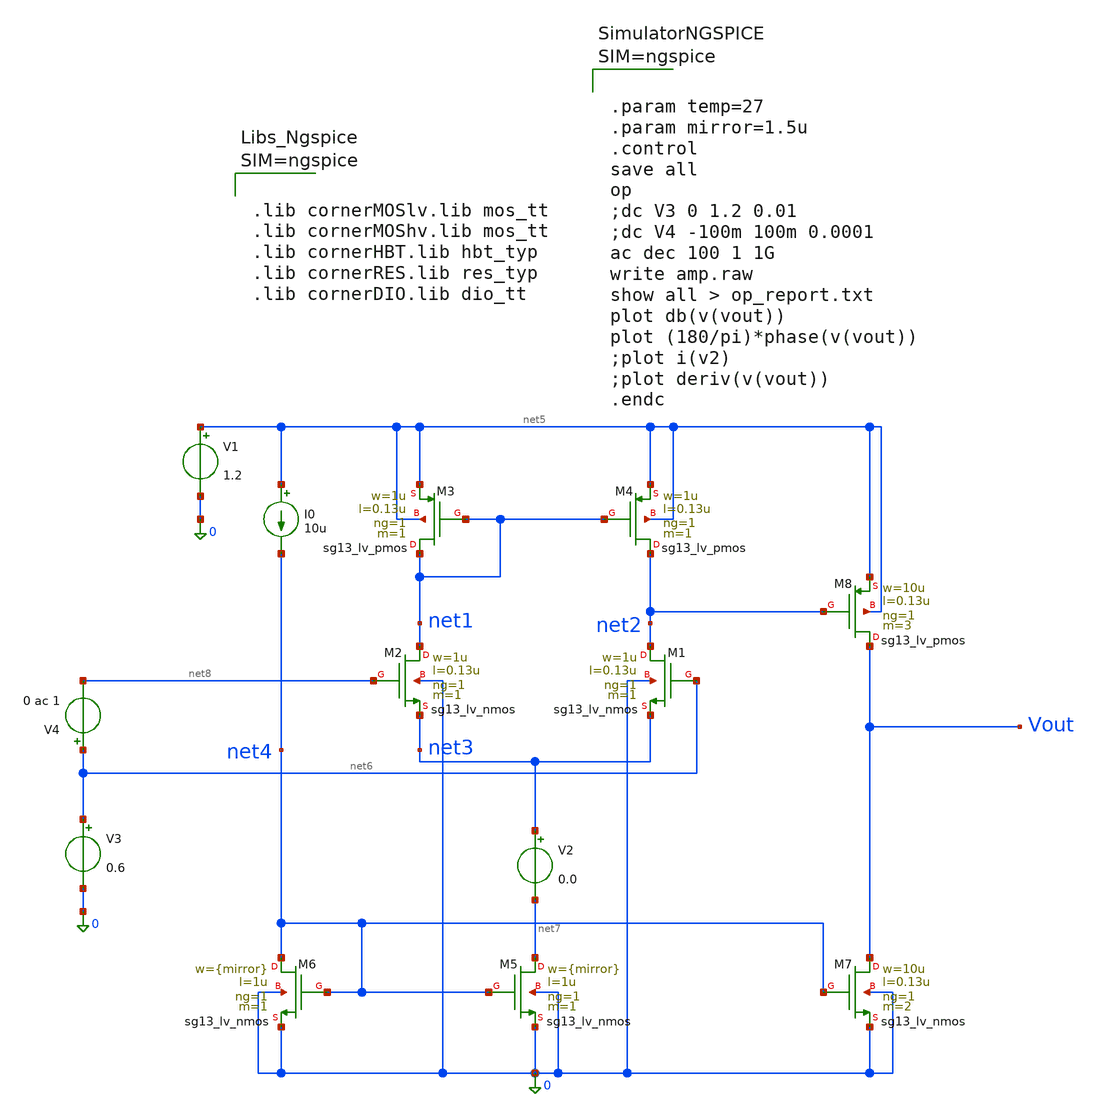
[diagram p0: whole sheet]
** sch_path: charge_pump/amp/amp.sch
**.subckt amp
XM1 net2 net6 net3 0 sg13_lv_nmos w=1u l=0.13u ng=1 m=1 mm_ok=1
XM2 net1 net8 net3 0 sg13_lv_nmos w=1u l=0.13u ng=1 m=1 mm_ok=1
XM3 net1 net1 net5 net5 sg13_lv_pmos w=1u l=0.13u ng=1 m=1 mm_ok=1
XM4 net2 net1 net5 net5 sg13_lv_pmos w=1u l=0.13u ng=1 m=1 mm_ok=1
I0 net5 net4 10u
XM5 net7 net4 0 0 sg13_lv_nmos w={mirror} l=1u ng=1 m=1 mm_ok=1
XM6 net4 net4 0 0 sg13_lv_nmos w={mirror} l=1u ng=1 m=1 mm_ok=1
XM7 Vout net4 0 0 sg13_lv_nmos w=10u l=0.13u ng=1 m=2 mm_ok=1
XM8 Vout net2 net5 net5 sg13_lv_pmos w=10u l=0.13u ng=1 m=3 mm_ok=1
V1 net5 0 1.2
V3 net6 0 0.6
V2 net3 net7 0.0
V4 net6 net8 0 ac 1
**** begin user architecture code



.lib cornerMOSlv.lib mos_tt
.lib cornerMOShv.lib mos_tt
.lib cornerHBT.lib hbt_typ
.lib cornerRES.lib res_typ
.lib cornerDIO.lib dio_tt






.param temp=27
.param mirror=1.5u
.control
save all
op
;dc V3 0 1.2 0.01
;dc V4 -100m 100m 0.0001
ac dec 100 1 1G
write amp.raw
show all > op_report.txt
plot db(v(vout))
plot (180/pi)*phase(v(vout))
;plot i(v2)
;plot deriv(v(vout))
.endc



**** end user architecture code
**.ends
.end
